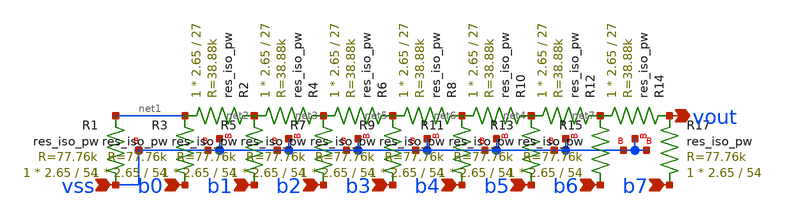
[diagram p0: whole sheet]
** sch_path: r2r.sch
**.subckt r2r vout vss b0 b1 b2 b3 b4 b5 b6 b7
*.opin vout
*.ipin vss
*.ipin b0
*.ipin b1
*.ipin b2
*.ipin b3
*.ipin b4
*.ipin b5
*.ipin b6
*.ipin b7
XR1 vss net1 vss sky130_fd_pr__res_iso_pw W=2.65 L=54 m=1
XR3 b0 net1 vss sky130_fd_pr__res_iso_pw W=2.65 L=54 m=1
XR5 b1 net2 vss sky130_fd_pr__res_iso_pw W=2.65 L=54 m=1
XR7 b2 net3 vss sky130_fd_pr__res_iso_pw W=2.65 L=54 m=1
XR13 b5 net4 vss sky130_fd_pr__res_iso_pw W=2.65 L=54 m=1
XR6 net3 net5 vss sky130_fd_pr__res_iso_pw W=2.65 L=27 m=1
XR4 net2 net3 vss sky130_fd_pr__res_iso_pw W=2.65 L=27 m=1
XR2 net1 net2 vss sky130_fd_pr__res_iso_pw W=2.65 L=27 m=1
XR9 b3 net5 vss sky130_fd_pr__res_iso_pw W=2.65 L=54 m=1
XR10 net6 net4 vss sky130_fd_pr__res_iso_pw W=2.65 L=27 m=1
XR11 b4 net6 vss sky130_fd_pr__res_iso_pw W=2.65 L=54 m=1
XR12 net4 net7 vss sky130_fd_pr__res_iso_pw W=2.65 L=27 m=1
XR8 net5 net6 vss sky130_fd_pr__res_iso_pw W=2.65 L=27 m=1
XR15 b6 net7 vss sky130_fd_pr__res_iso_pw W=2.65 L=54 m=1
XR14 net7 vout vss sky130_fd_pr__res_iso_pw W=2.65 L=27 m=1
XR17 b7 vout vss sky130_fd_pr__res_iso_pw W=2.65 L=54 m=1
**.ends
.end
